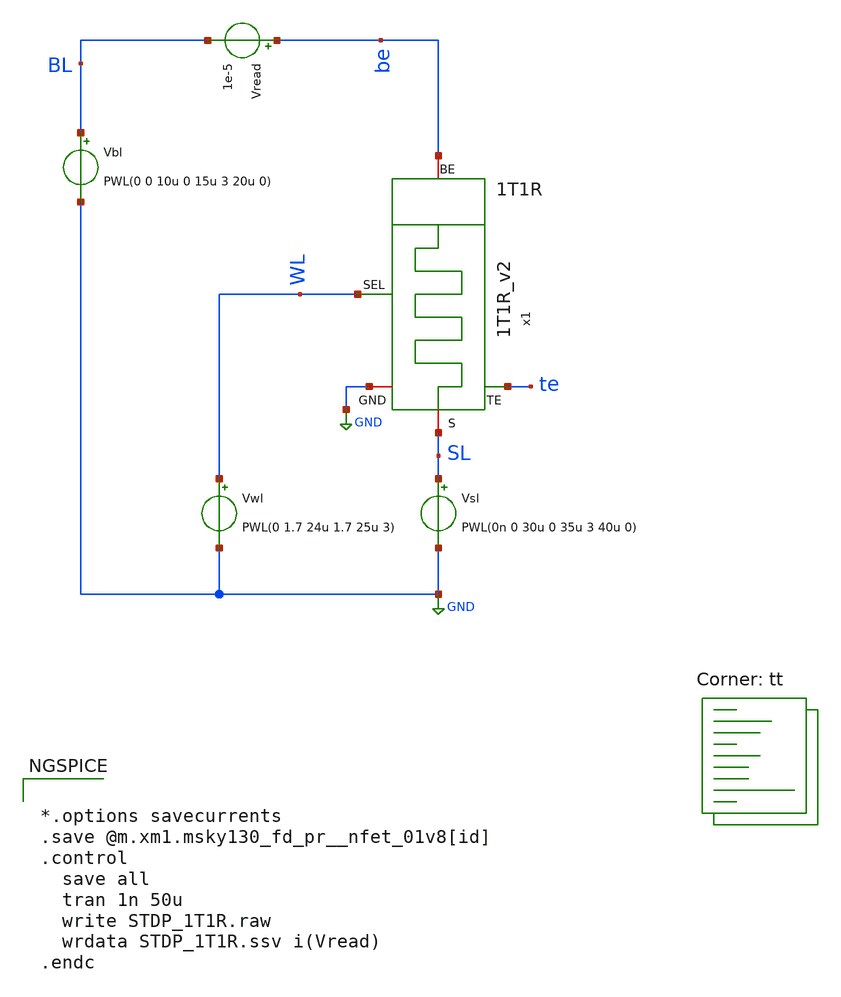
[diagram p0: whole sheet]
** sch_path: Ricardo/STDP_test/STDP_1T1R.sch
**.subckt STDP_1T1R
Vwl WL GND PWL(0 1.7 24u 1.7 25u 3)
Vbl BL GND PWL(0 0 10u 0 15u 3 20u 0)
Vread be BL 1e-5
Vsl SL GND PWL(0n 0 30u 0 35u 3 40u 0)
x1 be te WL GND SL 1T1R_v2
**** begin user architecture code


*.options savecurrents
.save @m.xm1.msky130_fd_pr__nfet_01v8[id]
.control
  save all
  tran 1n 50u
  write STDP_1T1R.raw
  wrdata STDP_1T1R.ssv i(Vread)
.endc


.lib $::SKYWATER_MODELS/sky130.lib.spice tt

** opencircuitdesign pdks install
.inc $::SKYWATER_MODELS/rram_v0.spice

**** end user architecture code
**.ends

* expanding   symbol:  /home/ricardo/RATT-repo/Proyectos_RATT/Proyectos_xschem/1T1R/1T1R_v2.sym # of
*+ pins=5
** sym_path: Ricardo/1T1R/1T1R_v2.sym
** sch_path: Ricardo/1T1R/1T1R_v2.sch
.subckt 1T1R_v2 BE TE SEL GND S
*.ipin SEL
*.iopin BE
*.iopin S
*.iopin GND
*.opin TE
XR1 TE BE rram_v0
XM1 TE SEL S GND sky130_fd_pr__nfet_01v8 L=0.15 W=1 nf=1 ad='int((nf+1)/2) * W/nf * 0.29' as='int((nf+2)/2) * W/nf * 0.29'
+ pd='2*int((nf+1)/2) * (W/nf + 0.29)' ps='2*int((nf+2)/2) * (W/nf + 0.29)' nrd='0.29 / W' nrs='0.29 / W'
+ sa=0 sb=0 sd=0 mult=1 m=1
.ends

.GLOBAL GND
.end
